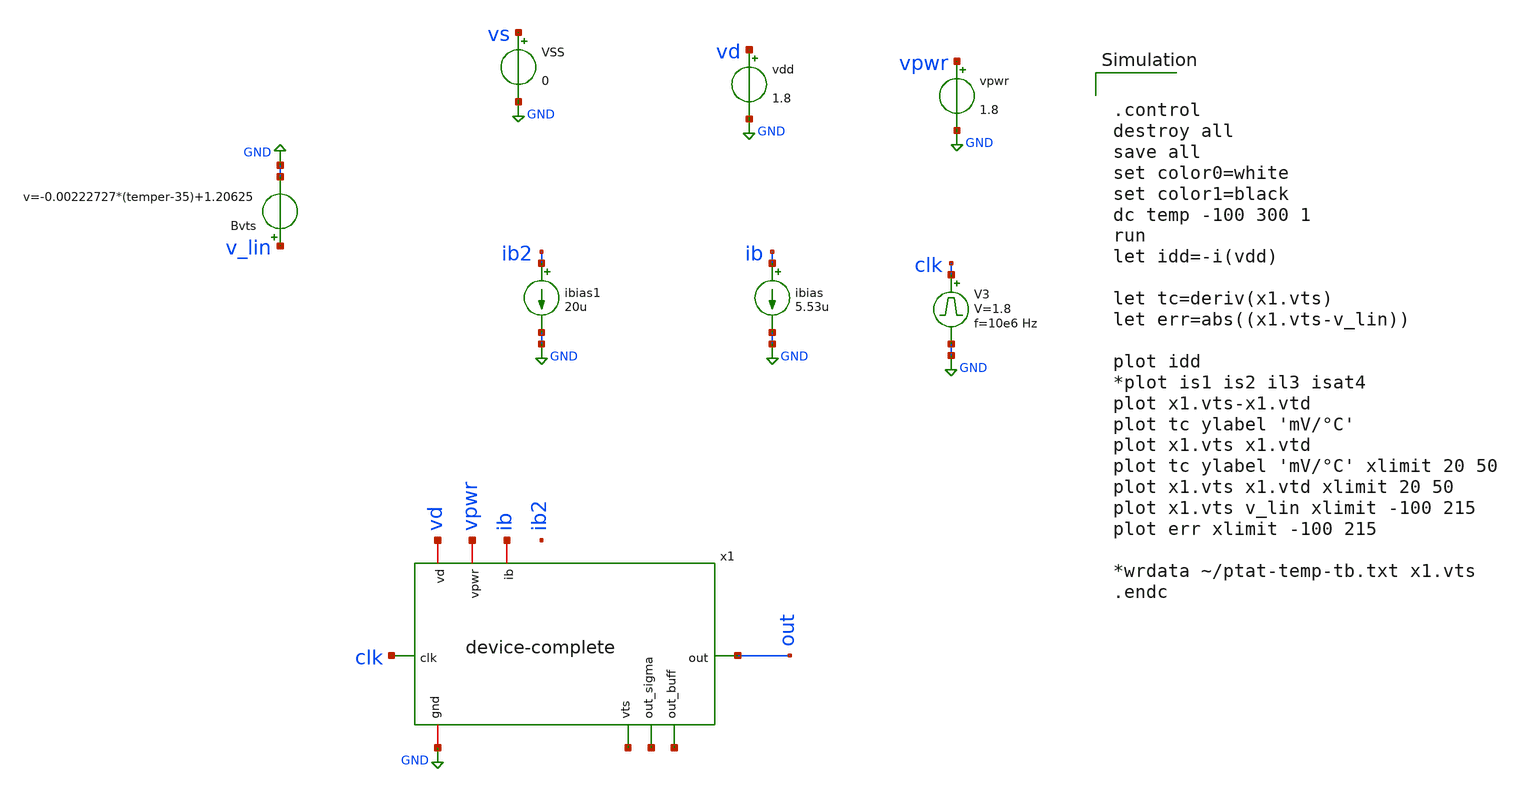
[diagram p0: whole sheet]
** sch_path: device-complete/xschem/device-complete_temp-tb .sch
**.subckt device-complete_temp-tb
vpwr vpwr GND 1.8
V3 clk GND pulse 0 1.8 '0.495/ 10e6 ' '0.01/10e6 ' '0.01/10e6 ' '0.49/10e6 ' '1/10e6 '
vdd vd GND 1.8
ibias ib GND 5.53u
VSS vs GND 0
ibias1 ib2 GND 20u
x1 vd clk out vpwr ib GND net1 net2 net3 device-complete
Bvts v_lin GND v=-0.00222727*(temper-35)+1.20625
**** begin user architecture code
 .lib $::SKYWATER_MODELS/sky130.lib.spice tt
.include $::SKYWATER_STDCELLS/sky130_fd_sc_hd.spice



.control
destroy all
save all
set color0=white
set color1=black
dc temp -100 300 1
run
let idd=-i(vdd)

let tc=deriv(x1.vts)
let err=abs((x1.vts-v_lin))

plot idd
*plot is1 is2 il3 isat4
plot x1.vts-x1.vtd
plot tc ylabel 'mV/°C'
plot x1.vts x1.vtd
plot tc ylabel 'mV/°C' xlimit 20 50
plot x1.vts x1.vtd xlimit 20 50
plot x1.vts v_lin xlimit -100 215
plot err xlimit -100 215

*wrdata ~/ptat-temp-tb.txt x1.vts
.endc


**** end user architecture code
**.ends
.GLOBAL GND
.end
